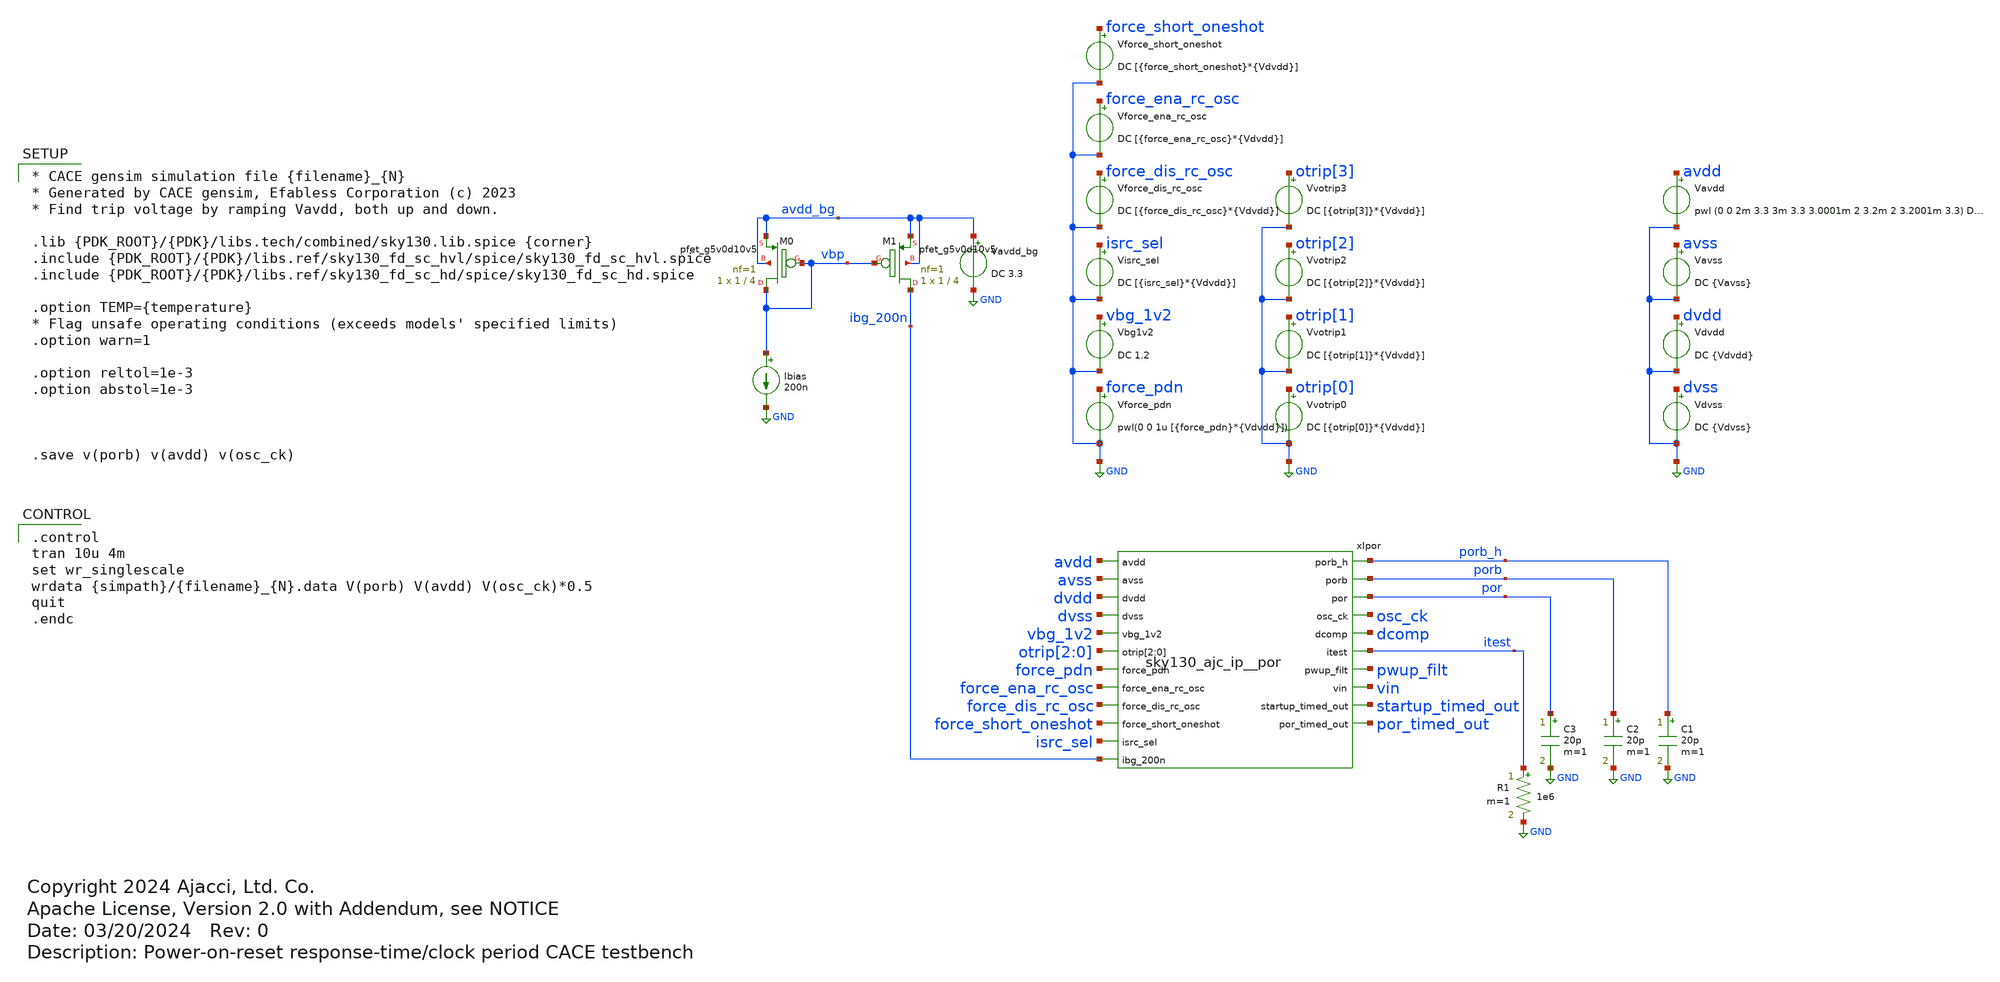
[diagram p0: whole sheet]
** sch_path: cace/transient.sch
* Copyright 2024 Ajacci, Ltd. Co.
* Apache License, Version 2.0 with Addendum, see NOTICE
**.subckt transient
Ibias vbp GND 200n
XM1 ibg_200n vbp avdd_bg avdd_bg sky130_fd_pr__pfet_g5v0d10v5 L=4 W=1 nf=1 ad='int((nf+1)/2) * W/nf * 0.29'
+ as='int((nf+2)/2) * W/nf * 0.29' pd='2*int((nf+1)/2) * (W/nf + 0.29)' ps='2*int((nf+2)/2) * (W/nf + 0.29)'
+ nrd='0.29 / W' nrs='0.29 / W' sa=0 sb=0 sd=0 mult=1 m=1
XM0 vbp vbp avdd_bg avdd_bg sky130_fd_pr__pfet_g5v0d10v5 L=4 W=1 nf=1 ad='int((nf+1)/2) * W/nf * 0.29'
+ as='int((nf+2)/2) * W/nf * 0.29' pd='2*int((nf+1)/2) * (W/nf + 0.29)' ps='2*int((nf+2)/2) * (W/nf + 0.29)'
+ nrd='0.29 / W' nrs='0.29 / W' sa=0 sb=0 sd=0 mult=1 m=1
R1 itest GND 1e6 m=1
Vavss avss GND DC {Vavss}
Vforce_pdn force_pdn GND pwl(0 0 1u [{force_pdn}*{Vdvdd}])
Vavdd avdd GND pwl (0 0 2m 3.3 3m 3.3 3.0001m 2 3.2m 2 3.2001m 3.3) DC {Vavdd}
.save i(vavdd)
Vbg1v2 vbg_1v2 GND DC 1.2
Vdvss dvss GND DC {Vdvss}
Vdvdd dvdd GND DC {Vdvdd}
.save i(vdvdd)
Vvotrip0 otrip[0] GND DC [{otrip[0]}*{Vdvdd}]
.save i(vvotrip0)
Vvotrip1 otrip[1] GND DC [{otrip[1]}*{Vdvdd}]
.save i(vvotrip1)
Vvotrip2 otrip[2] GND DC [{otrip[2]}*{Vdvdd}]
.save i(vvotrip2)
Vvotrip3 otrip[3] GND DC [{otrip[3]}*{Vdvdd}]
.save i(vvotrip3)
Visrc_sel isrc_sel GND DC [{isrc_sel}*{Vdvdd}]
Vavdd_bg avdd_bg GND DC 3.3
Vforce_dis_rc_osc force_dis_rc_osc GND DC [{force_dis_rc_osc}*{Vdvdd}]
Vforce_short_oneshot force_short_oneshot GND DC [{force_short_oneshot}*{Vdvdd}]
Vforce_ena_rc_osc force_ena_rc_osc GND DC [{force_ena_rc_osc}*{Vdvdd}]
xIpor avdd porb_h porb avss dvdd por dvss osc_ck vbg_1v2 dcomp otrip[2] otrip[1] otrip[0] itest
+ force_pdn pwup_filt vin force_ena_rc_osc force_dis_rc_osc startup_timed_out por_timed_out force_short_oneshot
+ isrc_sel ibg_200n sky130_ajc_ip__por
C1 porb_h GND 20p m=1
C2 porb GND 20p m=1
C3 por GND 20p m=1
**** begin user architecture code

* CACE gensim simulation file {filename}_{N}
* Generated by CACE gensim, Efabless Corporation (c) 2023
* Find trip voltage by ramping Vavdd, both up and down.

.lib {PDK_ROOT}/{PDK}/libs.tech/combined/sky130.lib.spice {corner}
.include {PDK_ROOT}/{PDK}/libs.ref/sky130_fd_sc_hvl/spice/sky130_fd_sc_hvl.spice
.include {PDK_ROOT}/{PDK}/libs.ref/sky130_fd_sc_hd/spice/sky130_fd_sc_hd.spice

.option TEMP={temperature}
* Flag unsafe operating conditions (exceeds models' specified limits)
.option warn=1

.option reltol=1e-3
.option abstol=1e-3



.save v(porb) v(avdd) v(osc_ck)



.control
tran 10u 4m
set wr_singlescale
wrdata {simpath}/{filename}_{N}.data V(porb) V(avdd) V(osc_ck)*0.5
quit
.endc


**** end user architecture code
**.ends
.GLOBAL GND
.end
